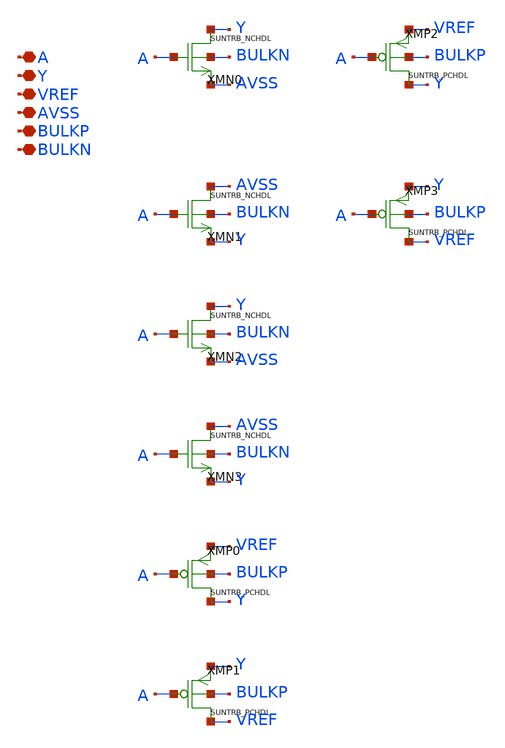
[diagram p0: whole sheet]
** sch_path: design/SUN_TRB_SKY130NM/SUNTRB_SWX4_CV.sch
**.subckt SUNTRB_SWX4_CV A Y VREF AVSS BULKP BULKN
*.iopin A
*.iopin Y
*.iopin VREF
*.iopin AVSS
*.iopin BULKP
*.iopin BULKN
XMN0 Y A AVSS BULKN SUNTRB_NCHDL xoffset=0 yoffset=0 angle=0
XMN1 AVSS A Y BULKN SUNTRB_NCHDL xoffset=0 yoffset=0 angle=0
XMN2 Y A AVSS BULKN SUNTRB_NCHDL xoffset=0 yoffset=0 angle=0
XMN3 AVSS A Y BULKN SUNTRB_NCHDL xoffset=0 yoffset=0 angle=0
XMP0 Y A VREF BULKP SUNTRB_PCHDL xoffset=0 yoffset=0 angle=0 M=1
XMP1 VREF A Y BULKP SUNTRB_PCHDL xoffset=0 yoffset=0 angle=0 M=1
XMP2 Y A VREF BULKP SUNTRB_PCHDL xoffset=0 yoffset=0 angle=0 M=1
XMP3 VREF A Y BULKP SUNTRB_PCHDL xoffset=0 yoffset=0 angle=0 M=1
**.ends
.end
